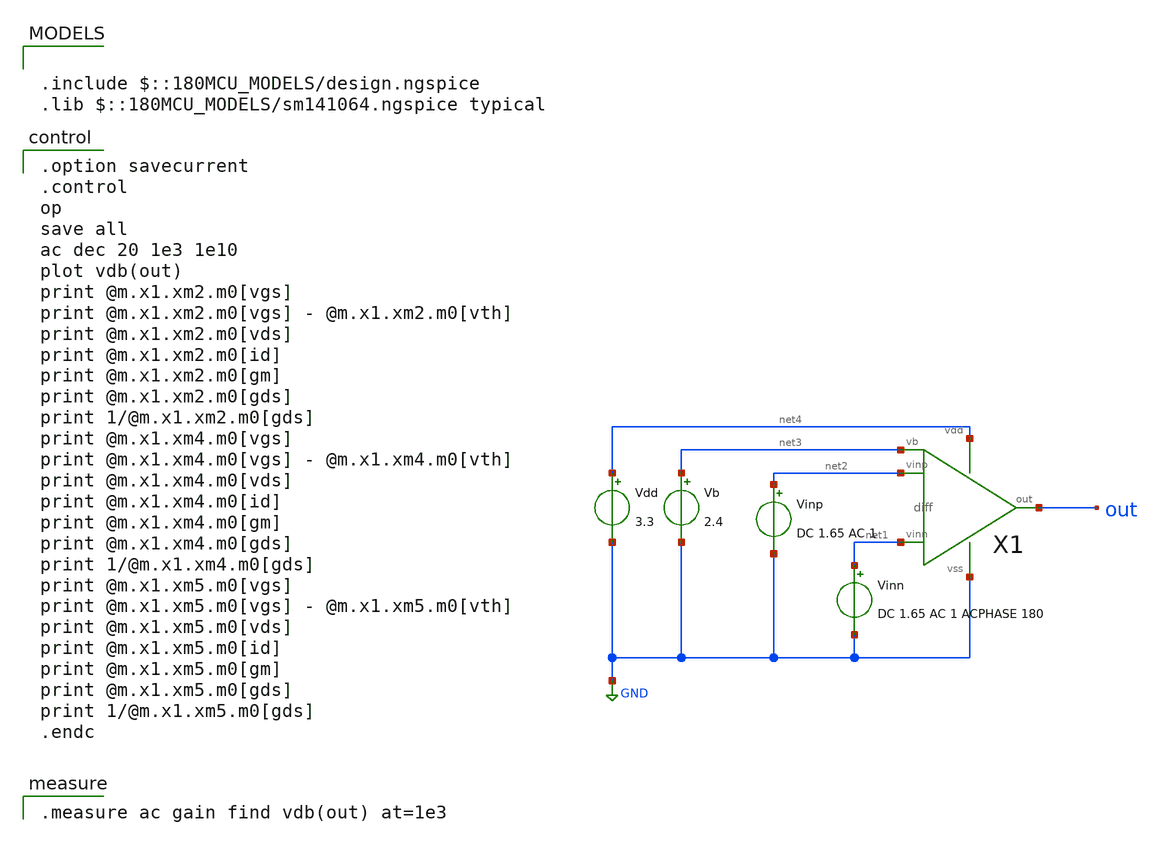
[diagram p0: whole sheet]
** sch_path: opamp/diff-stage_ac.sch
**.subckt diff-stage_ac
Vdd net4 GND 3.3
Vb net3 GND 2.4
Vinn net1 GND DC 1.65 AC 1 ACPHASE 180
Vinp net2 GND DC 1.65 AC 1
X1 net2 net1 out net4 GND net3 diff
**** begin user architecture code

.include $::180MCU_MODELS/design.ngspice
.lib $::180MCU_MODELS/sm141064.ngspice typical


.option savecurrent
.control
op
save all
ac dec 20 1e3 1e10
plot vdb(out)
print @m.x1.xm2.m0[vgs]
print @m.x1.xm2.m0[vgs] - @m.x1.xm2.m0[vth]
print @m.x1.xm2.m0[vds]
print @m.x1.xm2.m0[id]
print @m.x1.xm2.m0[gm]
print @m.x1.xm2.m0[gds]
print 1/@m.x1.xm2.m0[gds]
print @m.x1.xm4.m0[vgs]
print @m.x1.xm4.m0[vgs] - @m.x1.xm4.m0[vth]
print @m.x1.xm4.m0[vds]
print @m.x1.xm4.m0[id]
print @m.x1.xm4.m0[gm]
print @m.x1.xm4.m0[gds]
print 1/@m.x1.xm4.m0[gds]
print @m.x1.xm5.m0[vgs]
print @m.x1.xm5.m0[vgs] - @m.x1.xm5.m0[vth]
print @m.x1.xm5.m0[vds]
print @m.x1.xm5.m0[id]
print @m.x1.xm5.m0[gm]
print @m.x1.xm5.m0[gds]
print 1/@m.x1.xm5.m0[gds]
.endc


.measure ac gain find vdb(out) at=1e3

**** end user architecture code
**.ends
.GLOBAL GND
.end
